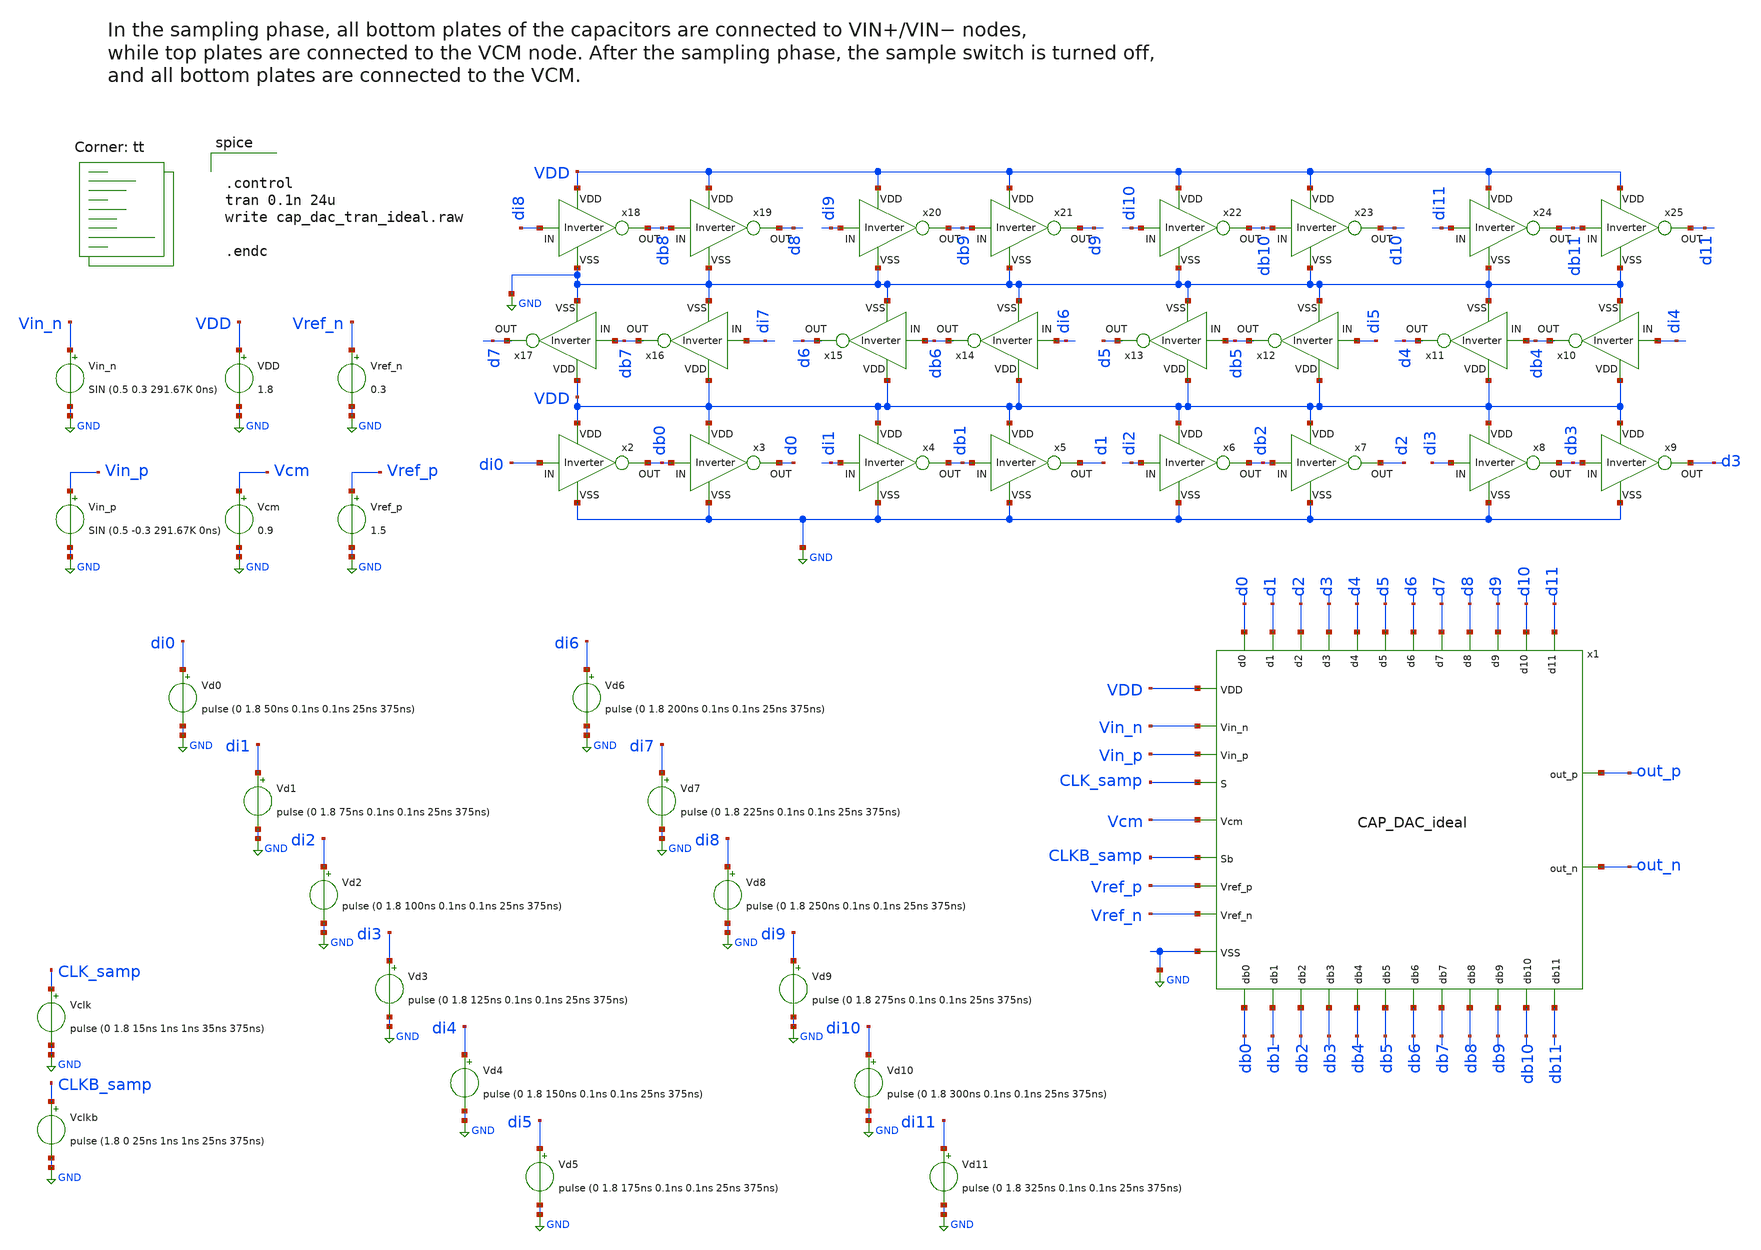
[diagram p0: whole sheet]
** sch_path: CAP_DAC_ideal_tb.sch
**.subckt CAP_DAC_ideal_tb
x2 VDD di0 db0 GND Inverter
x3 VDD db0 d0 GND Inverter
x4 VDD di1 db1 GND Inverter
x5 VDD db1 d1 GND Inverter
x6 VDD di2 db2 GND Inverter
x7 VDD db2 d2 GND Inverter
x8 VDD di3 db3 GND Inverter
x9 VDD db3 d3 GND Inverter
x10 VDD di4 db4 GND Inverter
x11 VDD db4 d4 GND Inverter
x12 VDD di5 db5 GND Inverter
x13 VDD db5 d5 GND Inverter
x14 VDD di6 db6 GND Inverter
x15 VDD db6 d6 GND Inverter
x16 VDD di7 db7 GND Inverter
x17 VDD db7 d7 GND Inverter
x18 VDD di8 db8 GND Inverter
x19 VDD db8 d8 GND Inverter
x20 VDD di9 db9 GND Inverter
x21 VDD db9 d9 GND Inverter
x22 VDD di10 db10 GND Inverter
x23 VDD db10 d10 GND Inverter
x24 VDD di11 db11 GND Inverter
x25 VDD db11 d11 GND Inverter
VDD VDD GND 1.8
Vclk CLK_samp GND pulse (0 1.8 15ns 1ns 1ns 35ns 375ns)
Vclkb CLKB_samp GND pulse (1.8 0 25ns 1ns 1ns 25ns 375ns)
Vcm Vcm GND 0.9
Vin_n Vin_n GND SIN (0.5 0.3 291.67K 0ns)
Vin_p Vin_p GND SIN (0.5 -0.3 291.67K 0ns)
Vref_n Vref_n GND 0.3
Vref_p Vref_p GND 1.5
Vd0 di0 GND pulse (0 1.8 50ns 0.1ns 0.1ns 25ns 375ns)
Vd1 di1 GND pulse (0 1.8 75ns 0.1ns 0.1ns 25ns 375ns)
Vd2 di2 GND pulse (0 1.8 100ns 0.1ns 0.1ns 25ns 375ns)
Vd3 di3 GND pulse (0 1.8 125ns 0.1ns 0.1ns 25ns 375ns)
Vd4 di4 GND pulse (0 1.8 150ns 0.1ns 0.1ns 25ns 375ns)
Vd5 di5 GND pulse (0 1.8 175ns 0.1ns 0.1ns 25ns 375ns)
Vd6 di6 GND pulse (0 1.8 200ns 0.1ns 0.1ns 25ns 375ns)
Vd7 di7 GND pulse (0 1.8 225ns 0.1ns 0.1ns 25ns 375ns)
Vd8 di8 GND pulse (0 1.8 250ns 0.1ns 0.1ns 25ns 375ns)
Vd9 di9 GND pulse (0 1.8 275ns 0.1ns 0.1ns 25ns 375ns)
Vd10 di10 GND pulse (0 1.8 300ns 0.1ns 0.1ns 25ns 375ns)
Vd11 di11 GND pulse (0 1.8 325ns 0.1ns 0.1ns 25ns 375ns)
x1 Vref_n Vin_n db0 db1 db2 VDD d3 db3 GND db4 d4 out_p Vcm db5 d5 CLK_samp db6 d6 CLKB_samp db7 d7
+ out_n d8 db8 d9 db9 db10 d10 db11 d11 Vin_p Vref_p d0 d1 d2 CAP_DAC_ideal
**** begin user architecture code
.lib $::SKYWATER_MODELS/sky130.lib.spice tt


.control
tran 0.1n 24u
write cap_dac_tran_ideal.raw

.endc


**** end user architecture code
**.ends

* expanding   symbol:  project/Inverter.sym # of pins=4
** sym_path: Inverter.sym
** sch_path: Inverter.sch
.subckt Inverter VDD IN OUT VSS
*.ipin IN
*.ipin VSS
*.ipin VDD
*.opin OUT
XM1 OUT IN VSS VSS sky130_fd_pr__nfet_01v8 L=0.3 W=1 nf=1 ad='int((nf+1)/2) * W/nf * 0.29' as='int((nf+2)/2) * W/nf * 0.29'
+ pd='2*int((nf+1)/2) * (W/nf + 0.29)' ps='2*int((nf+2)/2) * (W/nf + 0.29)' nrd='0.29 / W' nrs='0.29 / W'
+ sa=0 sb=0 sd=0 mult=1 m=1
XM2 OUT IN VDD VDD sky130_fd_pr__pfet_01v8 L=0.3 W=2 nf=1 ad='int((nf+1)/2) * W/nf * 0.29' as='int((nf+2)/2) * W/nf * 0.29'
+ pd='2*int((nf+1)/2) * (W/nf + 0.29)' ps='2*int((nf+2)/2) * (W/nf + 0.29)' nrd='0.29 / W' nrs='0.29 / W'
+ sa=0 sb=0 sd=0 mult=1 m=1
.ends


* expanding   symbol:  project/CAP_DAC_ideal.sym # of pins=35
** sym_path: CAP_DAC_ideal.sym
** sch_path: CAP_DAC_ideal.sch
.subckt CAP_DAC_ideal Vref_n Vin_n db0 db1 db2 VDD d3 db3 VSS db4 d4 out_p Vcm db5 d5 S db6 d6 Sb
+ db7 d7 out_n d8 db8 d9 db9 db10 d10 db11 d11 Vin_p Vref_p d0 d1 d2
*.ipin VDD
*.ipin VSS
*.ipin S
*.ipin Sb
*.ipin d3
*.ipin db3
*.ipin Vcm
*.opin out_p
*.opin out_n
*.ipin Vref_p
*.ipin Vref_n
*.ipin d0
*.ipin db0
*.ipin d1
*.ipin db1
*.ipin d2
*.ipin db2
*.ipin d5
*.ipin db5
*.ipin d4
*.ipin db4
*.ipin d7
*.ipin db7
*.ipin d6
*.ipin db6
*.ipin d9
*.ipin db9
*.ipin d8
*.ipin db8
*.ipin d11
*.ipin db11
*.ipin d10
*.ipin db10
*.ipin Vin_n
*.ipin Vin_p
x28 Vcm Sb S VDD VSS out_p transmission_gate
x29 Vcm Sb S VDD VSS out_n transmission_gate
x30 VDD Vref_n Vref_p VSS S Sb d0 db0 in_p_sampled net7 Network_Switch
x31 VDD Vref_n Vref_p VSS S Sb d1 db1 in_p_sampled net8 Network_Switch
x32 VDD Vref_n Vref_p VSS S Sb d2 db2 in_p_sampled net9 Network_Switch
x33 VDD Vref_n Vref_p VSS S Sb d3 db3 in_p_sampled net10 Network_Switch
x34 VDD Vref_n Vref_p VSS S Sb d4 db4 in_p_sampled net12 Network_Switch
x35 VDD Vref_n Vref_p VSS S Sb d5 db5 in_p_sampled net11 Network_Switch
x36 VDD Vref_n Vref_p VSS S Sb d6 db6 in_p_sampled net6 Network_Switch
x37 VDD Vref_n Vref_p VSS S Sb d7 db7 in_p_sampled net5 Network_Switch
x38 VDD Vref_n Vref_p VSS S Sb d8 db8 in_p_sampled net4 Network_Switch
x39 VDD Vref_n Vref_p VSS S Sb d9 db9 in_p_sampled net3 Network_Switch
x40 VDD Vref_n Vref_p VSS S Sb d10 db10 in_p_sampled net2 Network_Switch
x41 VDD Vref_n Vref_p VSS S Sb d11 db11 in_p_sampled net1 Network_Switch
x42 VDD Vref_n Vref_p VSS S Sb d0 db0 in_n_sampled node0 Network_Switch
x43 VDD Vref_n Vref_p VSS S Sb d1 db1 in_n_sampled net23 Network_Switch
x44 VDD Vref_n Vref_p VSS S Sb d2 db2 in_n_sampled net22 Network_Switch
x45 VDD Vref_n Vref_p VSS S Sb d3 db3 in_n_sampled net21 Network_Switch
x46 VDD Vref_n Vref_p VSS S Sb d4 db4 in_n_sampled net20 Network_Switch
x47 VDD Vref_n Vref_p VSS S Sb d5 db5 in_n_sampled net19 Network_Switch
x48 VDD Vref_n Vref_p VSS S Sb d6 db6 in_n_sampled net18 Network_Switch
x49 VDD Vref_n Vref_p VSS S Sb d7 db7 in_n_sampled net17 Network_Switch
x50 VDD Vref_n Vref_p VSS S Sb d8 db8 in_n_sampled net16 Network_Switch
x51 VDD Vref_n Vref_p VSS S Sb d9 db9 in_n_sampled net15 Network_Switch
x52 VDD Vref_n Vref_p VSS S Sb d10 db10 in_n_sampled net14 Network_Switch
x53 VDD Vref_n Vref_p VSS S Sb d11 db11 in_n_sampled net13 Network_Switch
x54 VDD Vin_n Sb S in_n_sampled VSS bootstrapped_switch
x55 VDD Vin_p Sb S in_p_sampled VSS bootstrapped_switch
x27 out_p Sb S VDD VSS out_n transmission_gate
C7 MSB_n net19 256f m=1
C8 MSB_n net20 128f m=1
C9 MSB_n net21 64f m=1
C10 MSB_n net22 32f m=1
C11 MSB_n net23 16f m=1
C12 MSB_n node0 8f m=1
C19 MSB_p net11 256f m=1
C20 MSB_p net12 128f m=1
C21 MSB_p net10 64f m=1
C22 MSB_p net9 32f m=1
C23 MSB_p net8 16f m=1
C24 MSB_p net7 8f m=1
C25 MSB_n Vref_n 8f m=1
C26 MSB_p Vref_n 8f m=1
C27 MSB_n out_p 8f m=1
C28 MSB_p out_n 8f m=1
C2 out_n net1 256f m=1
C3 out_n net2 128f m=1
C4 out_n net3 64f m=1
C5 out_n net4 32f m=1
C6 out_n net5 16f m=1
C14 out_n net6 8f m=1
C15 out_p net13 256f m=1
C16 out_p net14 128f m=1
C17 out_p net15 64f m=1
C18 out_p net16 32f m=1
C29 out_p net17 16f m=1
C30 out_p net18 8f m=1
x1 Vcm Sb S VDD VSS MSB_n transmission_gate
x2 Vcm Sb S VDD VSS MSB_p transmission_gate
.ends


* expanding   symbol:  project/transmission_gate.sym # of pins=6
** sym_path: transmission_gate.sym
** sch_path: transmission_gate.sch
.subckt transmission_gate in clkb clk VDD VSS out
*.ipin in
*.ipin clk
*.ipin clkb
*.opin out
*.ipin VDD
*.ipin VSS
XM1 out clk in VSS sky130_fd_pr__nfet_01v8 L=0.15 W=0.5 nf=1 ad='int((nf+1)/2) * W/nf * 0.29' as='int((nf+2)/2) * W/nf * 0.29'
+ pd='2*int((nf+1)/2) * (W/nf + 0.29)' ps='2*int((nf+2)/2) * (W/nf + 0.29)' nrd='0.29 / W' nrs='0.29 / W'
+ sa=0 sb=0 sd=0 mult=1 m=1
XM2 out clkb in VDD sky130_fd_pr__pfet_01v8 L=0.15 W=0.5 nf=1 ad='int((nf+1)/2) * W/nf * 0.29' as='int((nf+2)/2) * W/nf * 0.29'
+ pd='2*int((nf+1)/2) * (W/nf + 0.29)' ps='2*int((nf+2)/2) * (W/nf + 0.29)' nrd='0.29 / W' nrs='0.29 / W'
+ sa=0 sb=0 sd=0 mult=1 m=1
.ends


* expanding   symbol:  project/Network_Switch.sym # of pins=10
** sym_path: Network_Switch.sym
** sch_path: Network_Switch.sch
.subckt Network_Switch VDD ground Vref VSS S Sb d db Vin Vout
*.ipin ground
*.ipin Vref
*.ipin Vin
*.opin Vout
*.ipin VDD
*.ipin VSS
*.ipin S
*.ipin Sb
*.ipin d
*.ipin db
x1 ground d db VDD VSS net1 transmission_gate
x2 Vref db d VDD VSS net1 transmission_gate
x3 net1 S Sb VDD VSS Vout transmission_gate
x4 Vin Sb S VDD VSS Vout transmission_gate
.ends


* expanding   symbol:  project/bootstrapped_switch.sym # of pins=6
** sym_path: bootstrapped_switch.sym
** sch_path: bootstrapped_switch.sch
.subckt bootstrapped_switch VDD in clkb clk out VSS
*.ipin in
*.opin out
*.ipin VSS
*.ipin VDD
*.ipin clkb
*.ipin clk
XM1 net4 clkb net5 net5 sky130_fd_pr__nfet_01v8 L=0.15 W=2 nf=1 ad='int((nf+1)/2) * W/nf * 0.29' as='int((nf+2)/2) * W/nf * 0.29'
+ pd='2*int((nf+1)/2) * (W/nf + 0.29)' ps='2*int((nf+2)/2) * (W/nf + 0.29)' nrd='0.29 / W' nrs='0.29 / W'
+ sa=0 sb=0 sd=0 mult=1 m=1
XM2 in Vg net4 VSS sky130_fd_pr__nfet_01v8 L=1 W=0.5 nf=1 ad='int((nf+1)/2) * W/nf * 0.29' as='int((nf+2)/2) * W/nf * 0.29'
+ pd='2*int((nf+1)/2) * (W/nf + 0.29)' ps='2*int((nf+2)/2) * (W/nf + 0.29)' nrd='0.29 / W' nrs='0.29 / W'
+ sa=0 sb=0 sd=0 mult=1 m=1
XM3 Vp Vg net1 Vp sky130_fd_pr__pfet_01v8 L=0.15 W=2 nf=1 ad='int((nf+1)/2) * W/nf * 0.29' as='int((nf+2)/2) * W/nf * 0.29'
+ pd='2*int((nf+1)/2) * (W/nf + 0.29)' ps='2*int((nf+2)/2) * (W/nf + 0.29)' nrd='0.29 / W' nrs='0.29 / W'
+ sa=0 sb=0 sd=0 mult=1 m=1
XM5 out Vg in VSS sky130_fd_pr__nfet_01v8 L=0.15 W=30 nf=1 ad='int((nf+1)/2) * W/nf * 0.29' as='int((nf+2)/2) * W/nf * 0.29'
+ pd='2*int((nf+1)/2) * (W/nf + 0.29)' ps='2*int((nf+2)/2) * (W/nf + 0.29)' nrd='0.29 / W' nrs='0.29 / W'
+ sa=0 sb=0 sd=0 mult=1 m=1
XM6 out clkb in VDD sky130_fd_pr__pfet_01v8 L=0.15 W=30 nf=1 ad='int((nf+1)/2) * W/nf * 0.29' as='int((nf+2)/2) * W/nf * 0.29'
+ pd='2*int((nf+1)/2) * (W/nf + 0.29)' ps='2*int((nf+2)/2) * (W/nf + 0.29)' nrd='0.29 / W' nrs='0.29 / W'
+ sa=0 sb=0 sd=0 mult=1 m=1
XM8 net6 clkb net2 net2 sky130_fd_pr__nfet_01v8 L=0.15 W=0.5 nf=1 ad='int((nf+1)/2) * W/nf * 0.29' as='int((nf+2)/2) * W/nf * 0.29'
+ pd='2*int((nf+1)/2) * (W/nf + 0.29)' ps='2*int((nf+2)/2) * (W/nf + 0.29)' nrd='0.29 / W' nrs='0.29 / W'
+ sa=0 sb=0 sd=0 mult=1 m=1
XC1 net4 Vp sky130_fd_pr__cap_mim_m3_1 W=18 L=18 MF=10 m=10
XM7 Vg VDD net6 net6 sky130_fd_pr__nfet_01v8 L=0.15 W=0.5 nf=1 ad='int((nf+1)/2) * W/nf * 0.29' as='int((nf+2)/2) * W/nf * 0.29'
+ pd='2*int((nf+1)/2) * (W/nf + 0.29)' ps='2*int((nf+2)/2) * (W/nf + 0.29)' nrd='0.29 / W' nrs='0.29 / W'
+ sa=0 sb=0 sd=0 mult=1 m=1
XM4 Vg net3 Vp Vp sky130_fd_pr__pfet_01v8 L=0.15 W=0.5 nf=1 ad='int((nf+1)/2) * W/nf * 0.29' as='int((nf+2)/2) * W/nf * 0.29'
+ pd='2*int((nf+1)/2) * (W/nf + 0.29)' ps='2*int((nf+2)/2) * (W/nf + 0.29)' nrd='0.29 / W' nrs='0.29 / W'
+ sa=0 sb=0 sd=0 mult=1 m=1
XC2 out VSS sky130_fd_pr__cap_mim_m3_1 W=36 L=36 MF=20 m=20
XM10 net1 clk net7 net1 sky130_fd_pr__pfet_01v8 L=0.15 W=2 nf=1 ad='int((nf+1)/2) * W/nf * 0.29' as='int((nf+2)/2) * W/nf * 0.29'
+ pd='2*int((nf+1)/2) * (W/nf + 0.29)' ps='2*int((nf+2)/2) * (W/nf + 0.29)' nrd='0.29 / W' nrs='0.29 / W'
+ sa=0 sb=0 sd=0 mult=1 m=1
XM11 net5 clkb net8 net8 sky130_fd_pr__nfet_01v8 L=0.15 W=2 nf=1 ad='int((nf+1)/2) * W/nf * 0.29' as='int((nf+2)/2) * W/nf * 0.29'
+ pd='2*int((nf+1)/2) * (W/nf + 0.29)' ps='2*int((nf+2)/2) * (W/nf + 0.29)' nrd='0.29 / W' nrs='0.29 / W'
+ sa=0 sb=0 sd=0 mult=1 m=1
XM12 net7 clk VDD net7 sky130_fd_pr__pfet_01v8 L=0.15 W=2 nf=1 ad='int((nf+1)/2) * W/nf * 0.29' as='int((nf+2)/2) * W/nf * 0.29'
+ pd='2*int((nf+1)/2) * (W/nf + 0.29)' ps='2*int((nf+2)/2) * (W/nf + 0.29)' nrd='0.29 / W' nrs='0.29 / W'
+ sa=0 sb=0 sd=0 mult=1 m=1
XM13 net8 clkb VSS VSS sky130_fd_pr__nfet_01v8 L=0.15 W=2 nf=1 ad='int((nf+1)/2) * W/nf * 0.29' as='int((nf+2)/2) * W/nf * 0.29'
+ pd='2*int((nf+1)/2) * (W/nf + 0.29)' ps='2*int((nf+2)/2) * (W/nf + 0.29)' nrd='0.29 / W' nrs='0.29 / W'
+ sa=0 sb=0 sd=0 mult=1 m=1
XM14 net2 clkb VSS VSS sky130_fd_pr__nfet_01v8 L=0.15 W=0.5 nf=1 ad='int((nf+1)/2) * W/nf * 0.29' as='int((nf+2)/2) * W/nf * 0.29'
+ pd='2*int((nf+1)/2) * (W/nf + 0.29)' ps='2*int((nf+2)/2) * (W/nf + 0.29)' nrd='0.29 / W' nrs='0.29 / W'
+ sa=0 sb=0 sd=0 mult=1 m=1
XM15 net3 clk VDD VDD sky130_fd_pr__pfet_01v8 L=0.15 W=1 nf=1 ad='int((nf+1)/2) * W/nf * 0.29' as='int((nf+2)/2) * W/nf * 0.29'
+ pd='2*int((nf+1)/2) * (W/nf + 0.29)' ps='2*int((nf+2)/2) * (W/nf + 0.29)' nrd='0.29 / W' nrs='0.29 / W'
+ sa=0 sb=0 sd=0 mult=1 m=1
XM16 net3 clk net4 VSS sky130_fd_pr__nfet_01v8 L=1 W=0.5 nf=1 ad='int((nf+1)/2) * W/nf * 0.29' as='int((nf+2)/2) * W/nf * 0.29'
+ pd='2*int((nf+1)/2) * (W/nf + 0.29)' ps='2*int((nf+2)/2) * (W/nf + 0.29)' nrd='0.29 / W' nrs='0.29 / W'
+ sa=0 sb=0 sd=0 mult=1 m=1
XM17 net3 Vg net4 VSS sky130_fd_pr__nfet_01v8 L=0.15 W=2 nf=1 ad='int((nf+1)/2) * W/nf * 0.29' as='int((nf+2)/2) * W/nf * 0.29'
+ pd='2*int((nf+1)/2) * (W/nf + 0.29)' ps='2*int((nf+2)/2) * (W/nf + 0.29)' nrd='0.29 / W' nrs='0.29 / W'
+ sa=0 sb=0 sd=0 mult=1 m=1
.ends

.GLOBAL GND
.end
